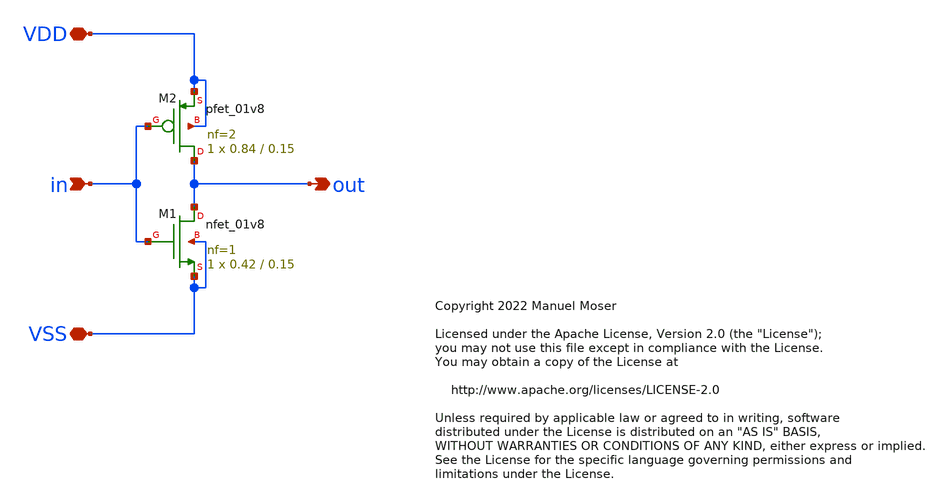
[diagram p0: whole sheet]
** sch_path: xschem/adc_inverter.sch
* Copyright 2022 Manuel Moser
* Licensed under the Apache License, Version 2.0 (the "License");
**.subckt adc_inverter VDD VSS in out
*.iopin VDD
*.iopin VSS
*.ipin in
*.opin out
XM2 out in VDD VDD sky130_fd_pr__pfet_01v8 L=0.15 W=0.84 nf=2 ad='int((nf+1)/2) * W/nf * 0.29' as='int((nf+2)/2) * W/nf * 0.29'
+ pd='2*int((nf+1)/2) * (W/nf + 0.29)' ps='2*int((nf+2)/2) * (W/nf + 0.29)' nrd='0.29 / W' nrs='0.29 / W'
+ sa=0 sb=0 sd=0 mult=1 m=1
XM1 out in VSS VSS sky130_fd_pr__nfet_01v8 L=0.15 W=0.42 nf=1 ad='int((nf+1)/2) * W/nf * 0.29' as='int((nf+2)/2) * W/nf * 0.29'
+ pd='2*int((nf+1)/2) * (W/nf + 0.29)' ps='2*int((nf+2)/2) * (W/nf + 0.29)' nrd='0.29 / W' nrs='0.29 / W'
+ sa=0 sb=0 sd=0 mult=1 m=1
**.ends
.end
